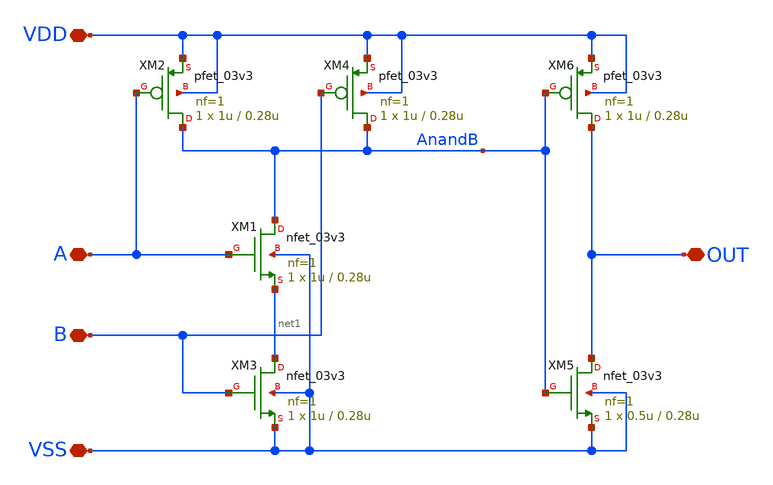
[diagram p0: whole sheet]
** sch_path: designs/libs/core_analog/qw_AND/qw_firsttest.sch
**.subckt qw_firsttest VDD VSS B A OUT
*.iopin VDD
*.iopin VSS
*.iopin B
*.iopin A
*.iopin OUT
XM1 AnandB A net1 VSS nfet_03v3 L=0.28u W=1u nf=1 ad='int((nf+1)/2) * W/nf * 0.18u' as='int((nf+2)/2) * W/nf * 0.18u'
+ pd='2*int((nf+1)/2) * (W/nf + 0.18u)' ps='2*int((nf+2)/2) * (W/nf + 0.18u)' nrd='0.18u / W' nrs='0.18u / W'
+ sa=0 sb=0 sd=0 m=1
XM2 AnandB A VDD VDD pfet_03v3 L=0.28u W=1u nf=1 ad='int((nf+1)/2) * W/nf * 0.18u' as='int((nf+2)/2) * W/nf * 0.18u'
+ pd='2*int((nf+1)/2) * (W/nf + 0.18u)' ps='2*int((nf+2)/2) * (W/nf + 0.18u)' nrd='0.18u / W' nrs='0.18u / W'
+ sa=0 sb=0 sd=0 m=1
XM3 net1 B VSS VSS nfet_03v3 L=0.28u W=1u nf=1 ad='int((nf+1)/2) * W/nf * 0.18u' as='int((nf+2)/2) * W/nf * 0.18u'
+ pd='2*int((nf+1)/2) * (W/nf + 0.18u)' ps='2*int((nf+2)/2) * (W/nf + 0.18u)' nrd='0.18u / W' nrs='0.18u / W'
+ sa=0 sb=0 sd=0 m=1
XM4 AnandB B VDD VDD pfet_03v3 L=0.28u W=1u nf=1 ad='int((nf+1)/2) * W/nf * 0.18u' as='int((nf+2)/2) * W/nf * 0.18u'
+ pd='2*int((nf+1)/2) * (W/nf + 0.18u)' ps='2*int((nf+2)/2) * (W/nf + 0.18u)' nrd='0.18u / W' nrs='0.18u / W'
+ sa=0 sb=0 sd=0 m=1
XM5 OUT AnandB VSS VSS nfet_03v3 L=0.28u W=0.5u nf=1 ad='int((nf+1)/2) * W/nf * 0.18u' as='int((nf+2)/2) * W/nf * 0.18u'
+ pd='2*int((nf+1)/2) * (W/nf + 0.18u)' ps='2*int((nf+2)/2) * (W/nf + 0.18u)' nrd='0.18u / W' nrs='0.18u / W'
+ sa=0 sb=0 sd=0 m=1
XM6 OUT AnandB VDD VDD pfet_03v3 L=0.28u W=1u nf=1 ad='int((nf+1)/2) * W/nf * 0.18u' as='int((nf+2)/2) * W/nf * 0.18u'
+ pd='2*int((nf+1)/2) * (W/nf + 0.18u)' ps='2*int((nf+2)/2) * (W/nf + 0.18u)' nrd='0.18u / W' nrs='0.18u / W'
+ sa=0 sb=0 sd=0 m=1
**.ends
.end
